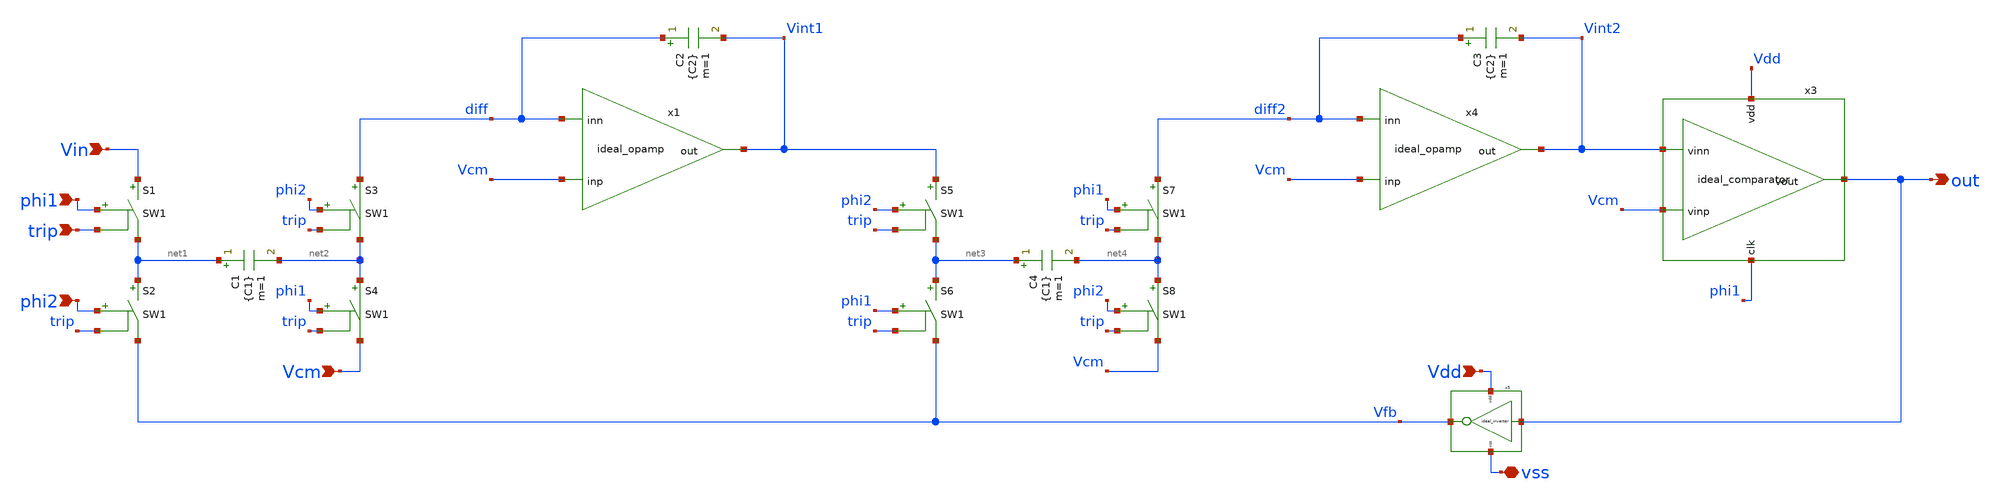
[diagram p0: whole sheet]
** sch_path: 2_ideal_circuits/second_order_modulator.sch
**.subckt second_order_modulator Vin phi1 trip phi2 Vcm Vdd vss out
*.ipin Vin
*.ipin phi1
*.ipin trip
*.ipin phi2
*.ipin Vcm
*.ipin Vdd
*.iopin vss
*.opin out
S1 Vin net1 phi1 trip SW1
S2 net1 Vfb phi2 trip SW1
S3 diff net2 phi2 trip SW1
S4 net2 Vcm phi1 trip SW1
x1 Vcm diff Vint1 ideal_opamp
C2 diff Vint1 {C2} m=1
C1 net1 net2 {C1} m=1
S5 Vint1 net3 phi2 trip SW1
S6 net3 Vfb phi1 trip SW1
S7 diff2 net4 phi1 trip SW1
S8 net4 Vcm phi2 trip SW1
x4 Vcm diff2 Vint2 ideal_opamp
C3 diff2 Vint2 {C2} m=1
C4 net3 net4 {C1} m=1
x3 Vdd out Vint2 Vcm phi1 ideal_comparator
x5 Vfb out vss Vdd ideal_inverter
**.ends

* expanding   symbol:  ideal_opamp.sym # of pins=3
** sym_path: ideal_opamp.sym
** sch_path: ideal_opamp.sch
.subckt ideal_opamp inp inn out
*.opin out
*.ipin inp
*.ipin inn
E1 out GND inp inn 1Meg
R1 out GND 100Meg m=1
.ends


* expanding   symbol:  ideal_comparator.sym # of pins=5
** sym_path: 2_ideal_circuits/ideal_comparator.sym
** sch_path: 2_ideal_circuits/ideal_comparator.sch
.subckt ideal_comparator Vdd Vout Vinn Vinp clk
*.ipin Vinp
*.ipin Vinn
*.opin Vout
*.iopin Vdd
*.iopin clk
E1 diff GND Vinp Vinn 1
S1 diff sample tp clk SW1
E2 net1 GND sample GND 1
C1 sample GND 100p m=1
S2 net1 hold clk tp SW1
C2 hold GND 100p m=1
B1 Vout GND V={v(hold)>0?v(Vdd):0}
Etp tp GND Vdd GND 0.5
**** begin user architecture code


.ic v(hold)=1 v(sample)=1


**** end user architecture code
.ends


* expanding   symbol:  ideal_inverter.sym # of pins=4
** sym_path: 2_ideal_circuits/ideal_inverter.sym
** sch_path: 2_ideal_circuits/ideal_inverter.sch
.subckt ideal_inverter out in vss vdd
*.iopin vdd
*.ipin in
*.opin out
*.iopin vss
B1 out GND V={v(in)>v(vdd)/2?v(vss):v(vdd)}
* noconn vdd
* noconn in
* noconn vss
.ends

.GLOBAL GND
**** begin user architecture code
.MODEL SW1 SW( VT=0.9 VH=0.01 RON=0.01 ROFF=10G )
**** end user architecture code
.end
